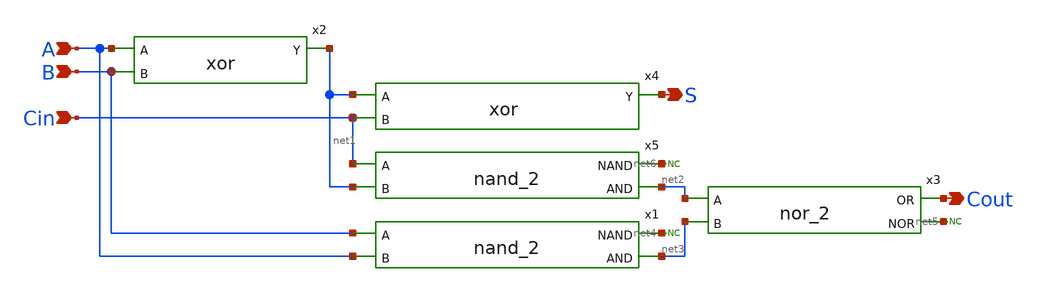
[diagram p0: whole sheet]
** sch_path: elements/full_adder.sch
**.subckt full_adder S A B Cin Cout
*.opin S
*.ipin A
*.ipin B
*.ipin Cin
*.opin Cout
x1 net4 net3 B A nand_2
x2 A B net1 xor
x3 net2 Cout net3 net5 nor_2
x4 net1 Cin S xor
x5 net6 net2 Cin net1 nand_2
* noconn #net5
* noconn #net4
* noconn #net6
**.ends
.end
